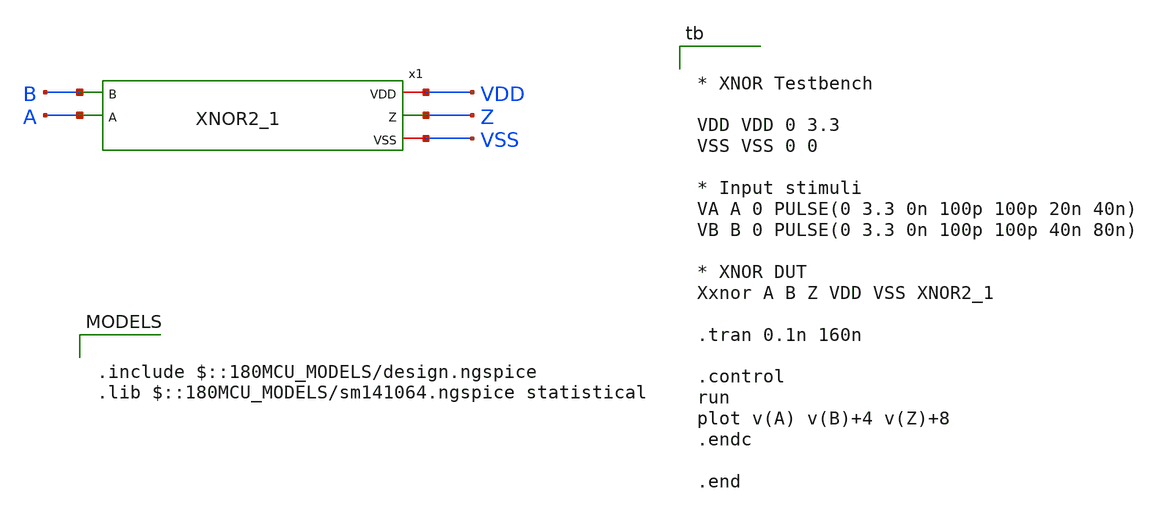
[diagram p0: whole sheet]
** sch_path: xschem/tb_mc_XNOR2_1.sch
**.subckt tb_mc_XNOR2_1
x1 VDD Z B A VSS XNOR2_1
**** begin user architecture code


* XNOR Testbench

VDD VDD 0 3.3
VSS VSS 0 0

* Input stimuli
VA A 0 PULSE(0 3.3 0n 100p 100p 20n 40n)
VB B 0 PULSE(0 3.3 0n 100p 100p 40n 80n)

* XNOR DUT
Xxnor A B Z VDD VSS XNOR2_1

.tran 0.1n 160n

.control
run
plot v(A) v(B)+4 v(Z)+8
.endc

.end


.include $::180MCU_MODELS/design.ngspice
.lib $::180MCU_MODELS/sm141064.ngspice statistical

**** end user architecture code
**.ends
.end
